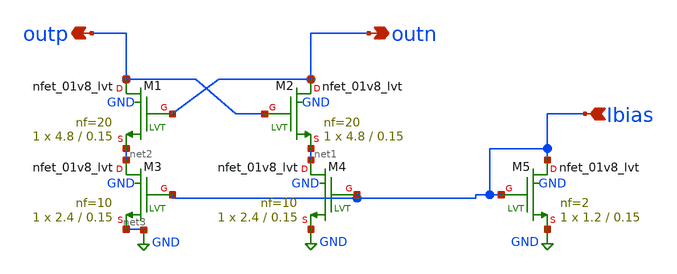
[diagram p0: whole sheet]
** sch_path: openfasoc/generators/lc-dco/xschem_rundir/diff_cross_mirror.sch
**.subckt diff_cross_mirror Ibias outn outp
*.ipin Ibias
*.opin outn
*.opin outp
XM1 outp outn net2 GND sky130_fd_pr__nfet_01v8_lvt L=0.15 W=4.8 nf=20 ad='int((nf+1)/2) * W/nf * 0.29'
+ as='int((nf+2)/2) * W/nf * 0.29' pd='2*int((nf+1)/2) * (W/nf + 0.29)' ps='2*int((nf+2)/2) * (W/nf + 0.29)'
+ nrd='0.29 / W' nrs='0.29 / W' sa=0 sb=0 sd=0 mult=1 m=1
XM2 outn outp net1 GND sky130_fd_pr__nfet_01v8_lvt L=0.15 W=4.8 nf=20 ad='int((nf+1)/2) * W/nf * 0.29'
+ as='int((nf+2)/2) * W/nf * 0.29' pd='2*int((nf+1)/2) * (W/nf + 0.29)' ps='2*int((nf+2)/2) * (W/nf + 0.29)'
+ nrd='0.29 / W' nrs='0.29 / W' sa=0 sb=0 sd=0 mult=1 m=1
XM4 net1 Ibias GND GND sky130_fd_pr__nfet_01v8_lvt L=0.15 W=2.4 nf=10 ad='int((nf+1)/2) * W/nf * 0.29'
+ as='int((nf+2)/2) * W/nf * 0.29' pd='2*int((nf+1)/2) * (W/nf + 0.29)' ps='2*int((nf+2)/2) * (W/nf + 0.29)'
+ nrd='0.29 / W' nrs='0.29 / W' sa=0 sb=0 sd=0 mult=1 m=1
XM5 Ibias Ibias GND GND sky130_fd_pr__nfet_01v8_lvt L=0.15 W=1.2 nf=2 ad='int((nf+1)/2) * W/nf * 0.29'
+ as='int((nf+2)/2) * W/nf * 0.29' pd='2*int((nf+1)/2) * (W/nf + 0.29)' ps='2*int((nf+2)/2) * (W/nf + 0.29)'
+ nrd='0.29 / W' nrs='0.29 / W' sa=0 sb=0 sd=0 mult=1 m=1
XM3 net2 Ibias net3 GND sky130_fd_pr__nfet_01v8_lvt L=0.15 W=2.4 nf=10 ad='int((nf+1)/2) * W/nf * 0.29'
+ as='int((nf+2)/2) * W/nf * 0.29' pd='2*int((nf+1)/2) * (W/nf + 0.29)' ps='2*int((nf+2)/2) * (W/nf + 0.29)'
+ nrd='0.29 / W' nrs='0.29 / W' sa=0 sb=0 sd=0 mult=1 m=1
**.ends
.GLOBAL GND
.end
